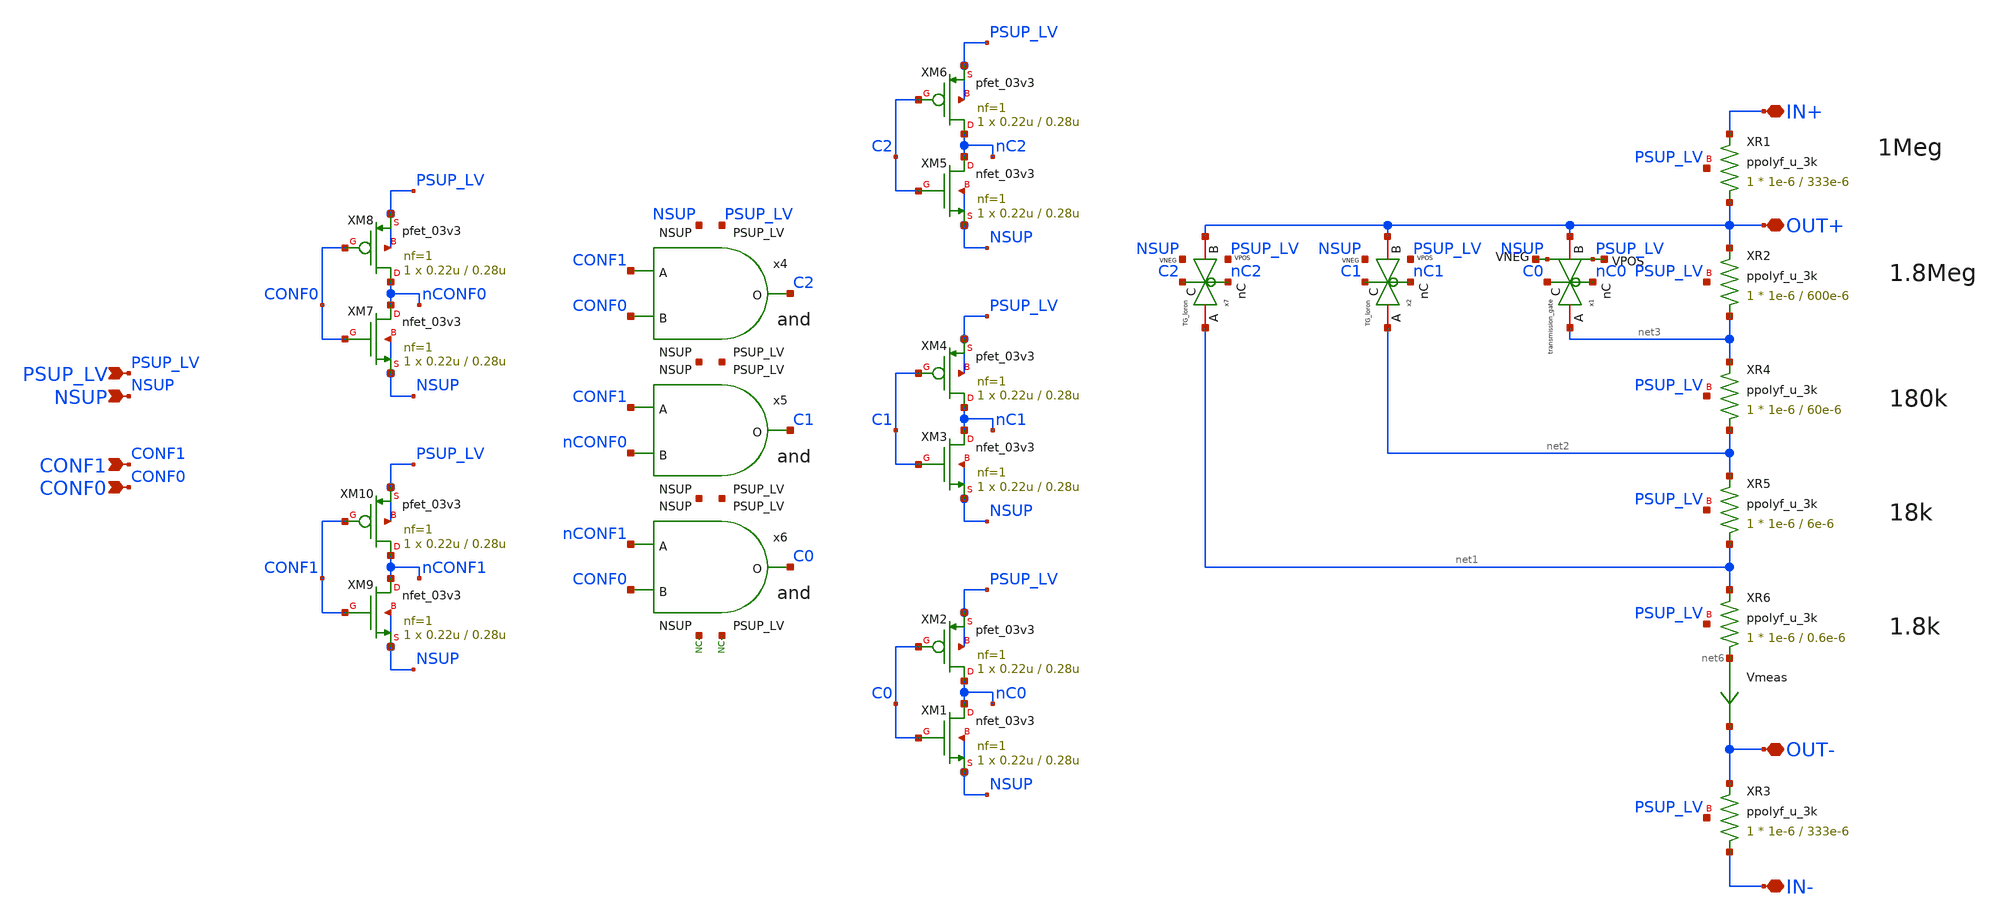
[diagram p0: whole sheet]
** sch_path: xschem/blocks/INA_gain_fb/INA_gain_fb.sch
**.subckt INA_gain_fb IN+ IN- OUT- OUT+ PSUP_LV NSUP CONF0 CONF1
*.iopin IN+
*.iopin IN-
*.iopin OUT-
*.iopin OUT+
*.ipin PSUP_LV
*.ipin NSUP
*.ipin CONF0
*.ipin CONF1
XR1 OUT+ IN+ PSUP_LV ppolyf_u_3k r_width=1e-6 r_length=333e-6 m=1
XR2 net3 OUT+ PSUP_LV ppolyf_u_3k r_width=1e-6 r_length=600e-6 m=1
XR3 IN- OUT- PSUP_LV ppolyf_u_3k r_width=1e-6 r_length=333e-6 m=1
XM1 nC0 C0 NSUP NSUP nfet_03v3 L=0.28u W=0.22u nf=1 ad='int((nf+1)/2) * W/nf * 0.18u' as='int((nf+2)/2) * W/nf * 0.18u'
+ pd='2*int((nf+1)/2) * (W/nf + 0.18u)' ps='2*int((nf+2)/2) * (W/nf + 0.18u)' nrd='0.18u / W' nrs='0.18u / W'
+ sa=0 sb=0 sd=0 m=1
XM2 nC0 C0 PSUP_LV PSUP_LV pfet_03v3 L=0.28u W=0.22u nf=1 ad='int((nf+1)/2) * W/nf * 0.18u' as='int((nf+2)/2) * W/nf * 0.18u'
+ pd='2*int((nf+1)/2) * (W/nf + 0.18u)' ps='2*int((nf+2)/2) * (W/nf + 0.18u)' nrd='0.18u / W' nrs='0.18u / W'
+ sa=0 sb=0 sd=0 m=1
XM3 nC1 C1 NSUP NSUP nfet_03v3 L=0.28u W=0.22u nf=1 ad='int((nf+1)/2) * W/nf * 0.18u' as='int((nf+2)/2) * W/nf * 0.18u'
+ pd='2*int((nf+1)/2) * (W/nf + 0.18u)' ps='2*int((nf+2)/2) * (W/nf + 0.18u)' nrd='0.18u / W' nrs='0.18u / W'
+ sa=0 sb=0 sd=0 m=1
XM4 nC1 C1 PSUP_LV PSUP_LV pfet_03v3 L=0.28u W=0.22u nf=1 ad='int((nf+1)/2) * W/nf * 0.18u' as='int((nf+2)/2) * W/nf * 0.18u'
+ pd='2*int((nf+1)/2) * (W/nf + 0.18u)' ps='2*int((nf+2)/2) * (W/nf + 0.18u)' nrd='0.18u / W' nrs='0.18u / W'
+ sa=0 sb=0 sd=0 m=1
XM5 nC2 C2 NSUP NSUP nfet_03v3 L=0.28u W=0.22u nf=1 ad='int((nf+1)/2) * W/nf * 0.18u' as='int((nf+2)/2) * W/nf * 0.18u'
+ pd='2*int((nf+1)/2) * (W/nf + 0.18u)' ps='2*int((nf+2)/2) * (W/nf + 0.18u)' nrd='0.18u / W' nrs='0.18u / W'
+ sa=0 sb=0 sd=0 m=1
XM6 nC2 C2 PSUP_LV PSUP_LV pfet_03v3 L=0.28u W=0.22u nf=1 ad='int((nf+1)/2) * W/nf * 0.18u' as='int((nf+2)/2) * W/nf * 0.18u'
+ pd='2*int((nf+1)/2) * (W/nf + 0.18u)' ps='2*int((nf+2)/2) * (W/nf + 0.18u)' nrd='0.18u / W' nrs='0.18u / W'
+ sa=0 sb=0 sd=0 m=1
x1 C0 net3 OUT+ nC0 net4 net5 transmission_gate
XR4 net2 net3 PSUP_LV ppolyf_u_3k r_width=1e-6 r_length=60e-6 m=1
XR5 net1 net2 PSUP_LV ppolyf_u_3k r_width=1e-6 r_length=6e-6 m=1
XR6 net6 net1 PSUP_LV ppolyf_u_3k r_width=1e-6 r_length=0.6e-6 m=1
x4 C2 CONF1 CONF0 PSUP_LV NSUP and
XM7 nCONF0 CONF0 NSUP NSUP nfet_03v3 L=0.28u W=0.22u nf=1 ad='int((nf+1)/2) * W/nf * 0.18u' as='int((nf+2)/2) * W/nf * 0.18u'
+ pd='2*int((nf+1)/2) * (W/nf + 0.18u)' ps='2*int((nf+2)/2) * (W/nf + 0.18u)' nrd='0.18u / W' nrs='0.18u / W'
+ sa=0 sb=0 sd=0 m=1
XM8 nCONF0 CONF0 PSUP_LV PSUP_LV pfet_03v3 L=0.28u W=0.22u nf=1 ad='int((nf+1)/2) * W/nf * 0.18u' as='int((nf+2)/2) * W/nf * 0.18u'
+ pd='2*int((nf+1)/2) * (W/nf + 0.18u)' ps='2*int((nf+2)/2) * (W/nf + 0.18u)' nrd='0.18u / W' nrs='0.18u / W'
+ sa=0 sb=0 sd=0 m=1
XM9 nCONF1 CONF1 NSUP NSUP nfet_03v3 L=0.28u W=0.22u nf=1 ad='int((nf+1)/2) * W/nf * 0.18u' as='int((nf+2)/2) * W/nf * 0.18u'
+ pd='2*int((nf+1)/2) * (W/nf + 0.18u)' ps='2*int((nf+2)/2) * (W/nf + 0.18u)' nrd='0.18u / W' nrs='0.18u / W'
+ sa=0 sb=0 sd=0 m=1
XM10 nCONF1 CONF1 PSUP_LV PSUP_LV pfet_03v3 L=0.28u W=0.22u nf=1 ad='int((nf+1)/2) * W/nf * 0.18u' as='int((nf+2)/2) * W/nf * 0.18u'
+ pd='2*int((nf+1)/2) * (W/nf + 0.18u)' ps='2*int((nf+2)/2) * (W/nf + 0.18u)' nrd='0.18u / W' nrs='0.18u / W'
+ sa=0 sb=0 sd=0 m=1
x5 C1 CONF1 nCONF0 PSUP_LV NSUP and
x6 C0 nCONF1 CONF0 PSUP_LV NSUP and
* noconn NSUP
* noconn PSUP_LV
Vmeas net6 OUT- 0
.save i(vmeas)
x7 C2 net1 OUT+ nC2 PSUP_LV NSUP TG_loron
x2 C1 net2 OUT+ nC1 PSUP_LV NSUP TG_loron
**.ends

* expanding   symbol:  blocks/transmission_gate/transmission_gate.sym # of pins=6
** sym_path: xschem/blocks/transmission_gate/transmission_gate.sym
** sch_path: xschem/blocks/transmission_gate/transmission_gate.sch
.subckt transmission_gate C A B nC VPOS VNEG
*.iopin A
*.iopin B
*.ipin C
*.ipin nC
*.ipin VPOS
*.ipin VNEG
XM3 A C B VNEG nfet_03v3 L=2u W=10u nf=1 ad='int((nf+1)/2) * W/nf * 0.18u' as='int((nf+2)/2) * W/nf * 0.18u'
+ pd='2*int((nf+1)/2) * (W/nf + 0.18u)' ps='2*int((nf+2)/2) * (W/nf + 0.18u)' nrd='0.18u / W' nrs='0.18u / W'
+ sa=0 sb=0 sd=0 m=2
XM4 A nC B VPOS pfet_03v3 L=2u W=10u nf=1 ad='int((nf+1)/2) * W/nf * 0.18u' as='int((nf+2)/2) * W/nf * 0.18u'
+ pd='2*int((nf+1)/2) * (W/nf + 0.18u)' ps='2*int((nf+2)/2) * (W/nf + 0.18u)' nrd='0.18u / W' nrs='0.18u / W'
+ sa=0 sb=0 sd=0 m=4
.ends


* expanding   symbol:  blocks/and/and.sym # of pins=7
** sym_path: xschem/blocks/and/and.sym
** sch_path: xschem/blocks/and/and.sch
.subckt and O A B PSUP_LV NSUP
*.ipin PSUP_LV
*.ipin NSUP
*.ipin A
*.ipin B
*.opin O
XM5 net1 B NSUP NSUP nfet_03v3 L=0.28u W=0.22u nf=1 ad='int((nf+1)/2) * W/nf * 0.18u' as='int((nf+2)/2) * W/nf * 0.18u'
+ pd='2*int((nf+1)/2) * (W/nf + 0.18u)' ps='2*int((nf+2)/2) * (W/nf + 0.18u)' nrd='0.18u / W' nrs='0.18u / W'
+ sa=0 sb=0 sd=0 m=1
XM1 net2 A net1 NSUP nfet_03v3 L=0.28u W=0.22u nf=1 ad='int((nf+1)/2) * W/nf * 0.18u' as='int((nf+2)/2) * W/nf * 0.18u'
+ pd='2*int((nf+1)/2) * (W/nf + 0.18u)' ps='2*int((nf+2)/2) * (W/nf + 0.18u)' nrd='0.18u / W' nrs='0.18u / W'
+ sa=0 sb=0 sd=0 m=1
XM2 net2 A PSUP_LV PSUP_LV pfet_03v3 L=0.28u W=0.22u nf=1 ad='int((nf+1)/2) * W/nf * 0.18u' as='int((nf+2)/2) * W/nf * 0.18u'
+ pd='2*int((nf+1)/2) * (W/nf + 0.18u)' ps='2*int((nf+2)/2) * (W/nf + 0.18u)' nrd='0.18u / W' nrs='0.18u / W'
+ sa=0 sb=0 sd=0 m=1
XM3 net2 B PSUP_LV PSUP_LV pfet_03v3 L=0.28u W=0.22u nf=1 ad='int((nf+1)/2) * W/nf * 0.18u' as='int((nf+2)/2) * W/nf * 0.18u'
+ pd='2*int((nf+1)/2) * (W/nf + 0.18u)' ps='2*int((nf+2)/2) * (W/nf + 0.18u)' nrd='0.18u / W' nrs='0.18u / W'
+ sa=0 sb=0 sd=0 m=1
XM4 O net2 PSUP_LV PSUP_LV pfet_03v3 L=0.28u W=0.22u nf=1 ad='int((nf+1)/2) * W/nf * 0.18u' as='int((nf+2)/2) * W/nf * 0.18u'
+ pd='2*int((nf+1)/2) * (W/nf + 0.18u)' ps='2*int((nf+2)/2) * (W/nf + 0.18u)' nrd='0.18u / W' nrs='0.18u / W'
+ sa=0 sb=0 sd=0 m=1
XM6 O net2 NSUP NSUP nfet_03v3 L=0.28u W=0.22u nf=1 ad='int((nf+1)/2) * W/nf * 0.18u' as='int((nf+2)/2) * W/nf * 0.18u'
+ pd='2*int((nf+1)/2) * (W/nf + 0.18u)' ps='2*int((nf+2)/2) * (W/nf + 0.18u)' nrd='0.18u / W' nrs='0.18u / W'
+ sa=0 sb=0 sd=0 m=1
.ends


* expanding   symbol:  blocks/TG_loron/TG_loron.sym # of pins=6
** sym_path: xschem/blocks/TG_loron/TG_loron.sym
** sch_path: xschem/blocks/TG_loron/TG_loron.sch
.subckt TG_loron C A B nC VPOS VNEG
*.iopin A
*.iopin B
*.ipin C
*.ipin nC
*.ipin VPOS
*.ipin VNEG
XM3 A C B VNEG nfet_03v3 L=2u W=10u nf=1 ad='int((nf+1)/2) * W/nf * 0.18u' as='int((nf+2)/2) * W/nf * 0.18u'
+ pd='2*int((nf+1)/2) * (W/nf + 0.18u)' ps='2*int((nf+2)/2) * (W/nf + 0.18u)' nrd='0.18u / W' nrs='0.18u / W'
+ sa=0 sb=0 sd=0 m=8
XM4 A nC B VPOS pfet_03v3 L=2u W=10u nf=1 ad='int((nf+1)/2) * W/nf * 0.18u' as='int((nf+2)/2) * W/nf * 0.18u'
+ pd='2*int((nf+1)/2) * (W/nf + 0.18u)' ps='2*int((nf+2)/2) * (W/nf + 0.18u)' nrd='0.18u / W' nrs='0.18u / W'
+ sa=0 sb=0 sd=0 m=16
.ends

.end
